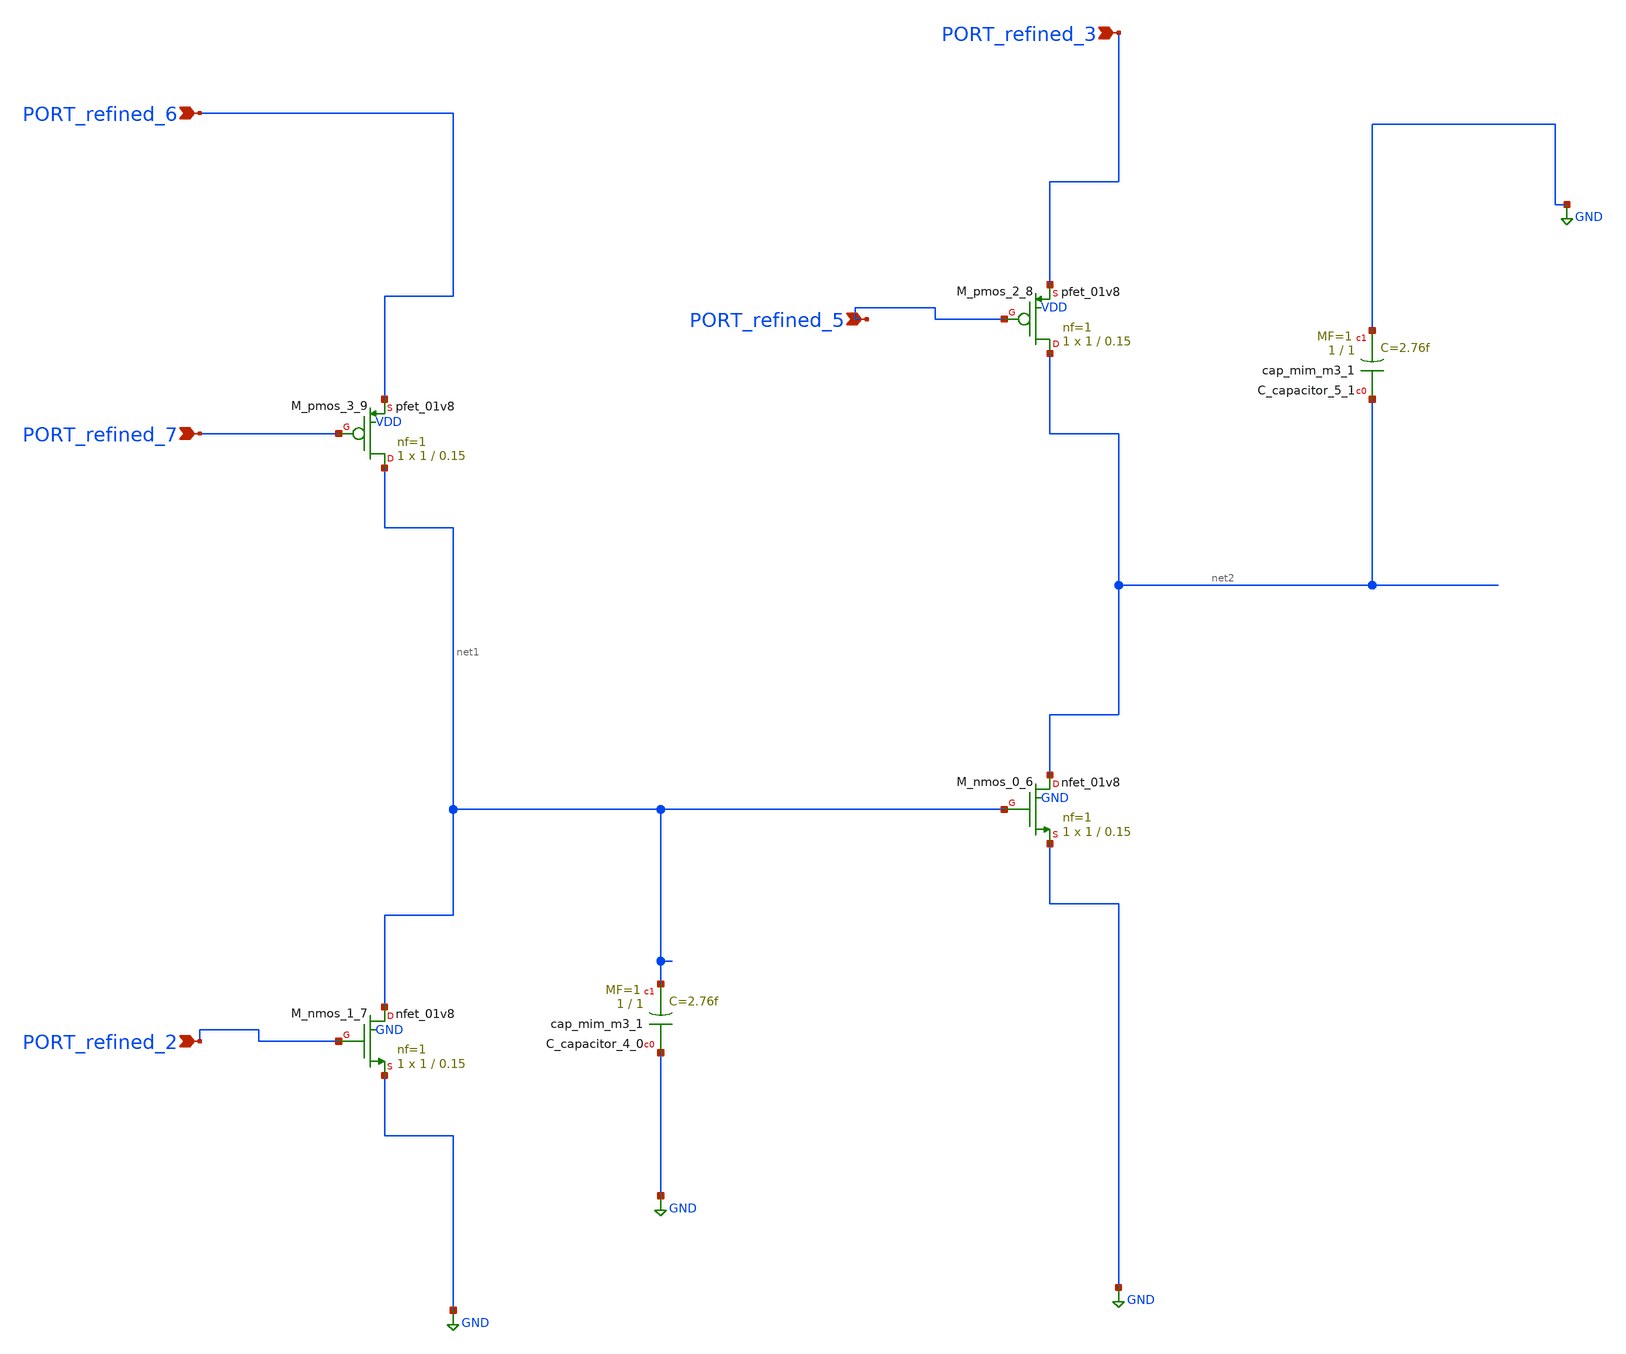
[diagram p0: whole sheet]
** sch_path: schematics/SchemGen/10_1007_s00034-017-0630-6_11_002_crop1.sch
**.subckt 10_1007_s00034-017-0630-6_11_002_crop1 PORT_refined_3 PORT_refined_7 PORT_refined_2
*+ PORT_refined_5 PORT_refined_6
*.ipin PORT_refined_3
*.ipin PORT_refined_7
*.ipin PORT_refined_2
*.ipin PORT_refined_5
*.ipin PORT_refined_6
XC_capacitor_4_0 GND net1 sky130_fd_pr__cap_mim_m3_1 W=1 L=1 MF=1 m=1
XC_capacitor_5_1 net2 GND sky130_fd_pr__cap_mim_m3_1 W=1 L=1 MF=1 m=1
XM_nmos_0_6 net2 net1 GND GND sky130_fd_pr__nfet_01v8 L=0.15 W=1 nf=1 ad='int((1 + 1)/2) * 1 / 1 * 0.29'
+ as='int((1 + 2)/2) * 1 / 1 * 0.29' pd='2*int((1 + 1)/2) * (1 / 1 + 0.29)' ps='2*int((1 + 2)/2) * (1 / 1 + 0.29)'
+ nrd='0.29 / 1 ' nrs='0.29 / 1 ' sa=0 sb=0 sd=0 mult=1 m=1
XM_nmos_1_7 net1 PORT_refined_2 GND GND sky130_fd_pr__nfet_01v8 L=0.15 W=1 nf=1 ad='int((1 + 1)/2) * 1 / 1 * 0.29'
+ as='int((1 + 2)/2) * 1 / 1 * 0.29' pd='2*int((1 + 1)/2) * (1 / 1 + 0.29)' ps='2*int((1 + 2)/2) * (1 / 1 + 0.29)'
+ nrd='0.29 / 1 ' nrs='0.29 / 1 ' sa=0 sb=0 sd=0 mult=1 m=1
XM_pmos_2_8 net2 PORT_refined_5 PORT_refined_3 VDD sky130_fd_pr__pfet_01v8 L=0.15 W=1 nf=1 ad='int((1 + 1)/2) * 1 / 1 * 0.29'
+ as='int((1 + 2)/2) * 1 / 1 * 0.29' pd='2*int((1 + 1)/2) * (1 / 1 + 0.29)' ps='2*int((1 + 2)/2) * (1 / 1 + 0.29)'
+ nrd='0.29 / 1 ' nrs='0.29 / 1 ' sa=0 sb=0 sd=0 mult=1 m=1
XM_pmos_3_9 net1 PORT_refined_7 PORT_refined_6 VDD sky130_fd_pr__pfet_01v8 L=0.15 W=1 nf=1 ad='int((1 + 1)/2) * 1 / 1 * 0.29'
+ as='int((1 + 2)/2) * 1 / 1 * 0.29' pd='2*int((1 + 1)/2) * (1 / 1 + 0.29)' ps='2*int((1 + 2)/2) * (1 / 1 + 0.29)'
+ nrd='0.29 / 1 ' nrs='0.29 / 1 ' sa=0 sb=0 sd=0 mult=1 m=1
**.ends
.GLOBAL GND
.end
